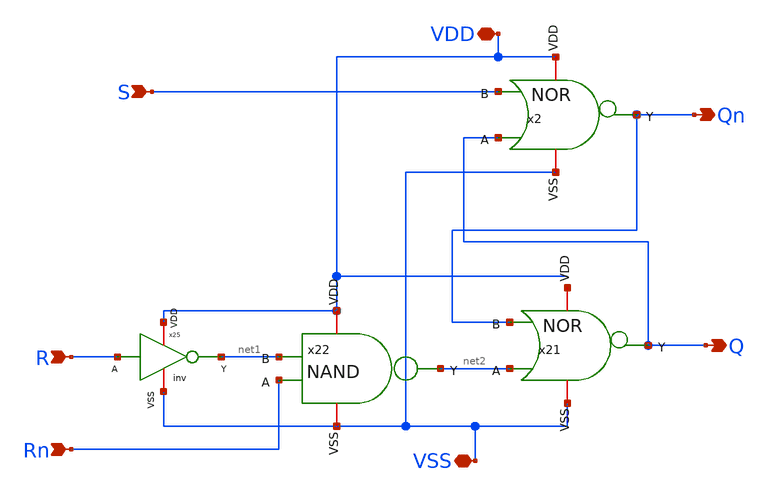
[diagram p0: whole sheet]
** sch_path: xschem/LatchJK.sch
**.subckt LatchJK Qn Rn VDD VSS R S Q
*.opin Qn
*.ipin Rn
*.iopin VDD
*.iopin VSS
*.ipin R
*.ipin S
*.opin Q
x2 VDD S Q Qn VSS NOR
x21 net3 Qn net2 Q VSS NOR
x22 VDD net1 Rn net2 VSS NAND
x25 VDD net1 R VSS inv
**.ends
.end
